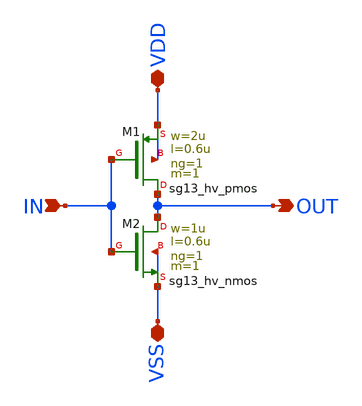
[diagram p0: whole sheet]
** sch_path: real_circuit/sandbox/real_inv.sch
**.subckt real_inv VDD VSS IN OUT
*.iopin VDD
*.iopin VSS
*.ipin IN
*.opin OUT
XM1 OUT IN VDD VDD sg13_hv_pmos w=2u l=0.6u ng=1 m=1 mm_ok=1
XM2 OUT IN VSS VSS sg13_hv_nmos w=1u l=0.6u ng=1 m=1 mm_ok=1
**.ends
.end
